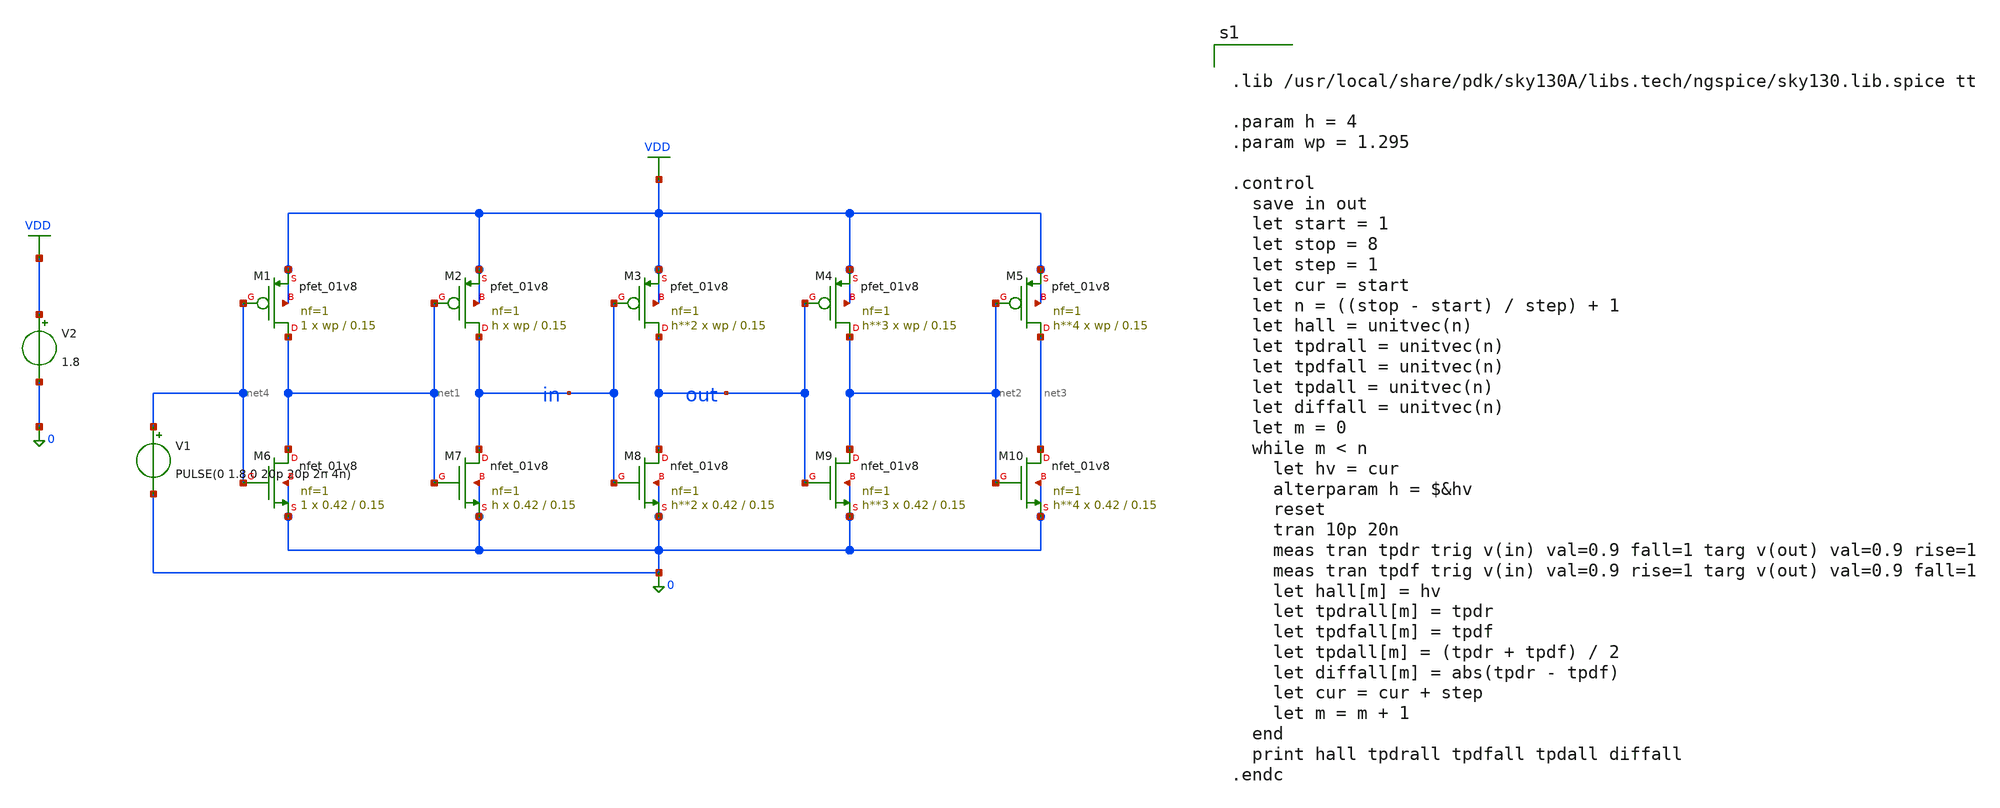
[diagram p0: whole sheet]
** sch_path: static_cmos/logicaleffort/inv.sch
**.subckt inv
V1 net4 0 PULSE(0 1.8 0 20p 20p 2n 4n)
V2 VDD 0 1.8
XM1 net1 net4 VDD VDD sky130_fd_pr__pfet_01v8 L=0.15 W=wp nf=1 ad='int((1 + 1)/2) * wp / 1 * 0.29' as='int((1 + 2)/2) * wp / 1 * 0.29'
+ pd='2*int((1 + 1)/2) * (wp / 1 + 0.29)' ps='2*int((1 + 2)/2) * (wp / 1 + 0.29)' nrd='0.29 / wp ' nrs='0.29 / wp '
+ sa=0 sb=0 sd=0 mult=1 m=1
XM2 in net1 VDD VDD sky130_fd_pr__pfet_01v8 L=0.15 W=wp nf=1 ad='int((1 + 1)/2) * wp / 1 * 0.29' as='int((1 + 2)/2) * wp / 1 * 0.29'
+ pd='2*int((1 + 1)/2) * (wp / 1 + 0.29)' ps='2*int((1 + 2)/2) * (wp / 1 + 0.29)' nrd='0.29 / wp ' nrs='0.29 / wp '
+ sa=0 sb=0 sd=0 mult=h m=h
XM3 out in VDD VDD sky130_fd_pr__pfet_01v8 L=0.15 W=wp nf=1 ad='int((1 + 1)/2) * wp / 1 * 0.29' as='int((1 + 2)/2) * wp / 1 * 0.29'
+ pd='2*int((1 + 1)/2) * (wp / 1 + 0.29)' ps='2*int((1 + 2)/2) * (wp / 1 + 0.29)' nrd='0.29 / wp ' nrs='0.29 / wp '
+ sa=0 sb=0 sd=0 mult=h**2 m=h**2
XM4 net2 out VDD VDD sky130_fd_pr__pfet_01v8 L=0.15 W=wp nf=1 ad='int((1 + 1)/2) * wp / 1 * 0.29' as='int((1 + 2)/2) * wp / 1 * 0.29'
+ pd='2*int((1 + 1)/2) * (wp / 1 + 0.29)' ps='2*int((1 + 2)/2) * (wp / 1 + 0.29)' nrd='0.29 / wp ' nrs='0.29 / wp '
+ sa=0 sb=0 sd=0 mult=h**3 m=h**3
XM5 net3 net2 VDD VDD sky130_fd_pr__pfet_01v8 L=0.15 W=wp nf=1 ad='int((1 + 1)/2) * wp / 1 * 0.29' as='int((1 + 2)/2) * wp / 1 * 0.29'
+ pd='2*int((1 + 1)/2) * (wp / 1 + 0.29)' ps='2*int((1 + 2)/2) * (wp / 1 + 0.29)' nrd='0.29 / wp ' nrs='0.29 / wp '
+ sa=0 sb=0 sd=0 mult=h**4 m=h**4
XM6 net1 net4 0 0 sky130_fd_pr__nfet_01v8 L=0.15 W=0.42 nf=1 ad='int((1 + 1)/2) * 0.42 / 1 * 0.29' as='int((1 + 2)/2) * 0.42 / 1 * 0.29'
+ pd='2*int((1 + 1)/2) * (0.42 / 1 + 0.29)' ps='2*int((1 + 2)/2) * (0.42 / 1 + 0.29)' nrd='0.29 / 0.42 '
+ nrs='0.29 / 0.42 ' sa=0 sb=0 sd=0 mult=1 m=1
XM7 in net1 0 0 sky130_fd_pr__nfet_01v8 L=0.15 W=0.42 nf=1 ad='int((1 + 1)/2) * 0.42 / 1 * 0.29' as='int((1 + 2)/2) * 0.42 / 1 * 0.29'
+ pd='2*int((1 + 1)/2) * (0.42 / 1 + 0.29)' ps='2*int((1 + 2)/2) * (0.42 / 1 + 0.29)' nrd='0.29 / 0.42 '
+ nrs='0.29 / 0.42 ' sa=0 sb=0 sd=0 mult=h m=h
XM8 out in 0 0 sky130_fd_pr__nfet_01v8 L=0.15 W=0.42 nf=1 ad='int((1 + 1)/2) * 0.42 / 1 * 0.29' as='int((1 + 2)/2) * 0.42 / 1 * 0.29'
+ pd='2*int((1 + 1)/2) * (0.42 / 1 + 0.29)' ps='2*int((1 + 2)/2) * (0.42 / 1 + 0.29)' nrd='0.29 / 0.42 '
+ nrs='0.29 / 0.42 ' sa=0 sb=0 sd=0 mult=h**2 m=h**2
XM9 net2 out 0 0 sky130_fd_pr__nfet_01v8 L=0.15 W=0.42 nf=1 ad='int((1 + 1)/2) * 0.42 / 1 * 0.29' as='int((1 + 2)/2) * 0.42 / 1 * 0.29'
+ pd='2*int((1 + 1)/2) * (0.42 / 1 + 0.29)' ps='2*int((1 + 2)/2) * (0.42 / 1 + 0.29)' nrd='0.29 / 0.42 '
+ nrs='0.29 / 0.42 ' sa=0 sb=0 sd=0 mult=h**3 m=h**3
XM10 net3 net2 0 0 sky130_fd_pr__nfet_01v8 L=0.15 W=0.42 nf=1 ad='int((1 + 1)/2) * 0.42 / 1 * 0.29' as='int((1 + 2)/2) * 0.42 / 1 * 0.29'
+ pd='2*int((1 + 1)/2) * (0.42 / 1 + 0.29)' ps='2*int((1 + 2)/2) * (0.42 / 1 + 0.29)' nrd='0.29 / 0.42 '
+ nrs='0.29 / 0.42 ' sa=0 sb=0 sd=0 mult=h**4 m=h**4
**** begin user architecture code


.lib /usr/local/share/pdk/sky130A/libs.tech/ngspice/sky130.lib.spice tt

.param h = 4
.param wp = 1.295

.control
  save in out
  let start = 1
  let stop = 8
  let step = 1
  let cur = start
  let n = ((stop - start) / step) + 1
  let hall = unitvec(n)
  let tpdrall = unitvec(n)
  let tpdfall = unitvec(n)
  let tpdall = unitvec(n)
  let diffall = unitvec(n)
  let m = 0
  while m < n
    let hv = cur
    alterparam h = $&hv
    reset
    tran 10p 20n
    meas tran tpdr trig v(in) val=0.9 fall=1 targ v(out) val=0.9 rise=1
    meas tran tpdf trig v(in) val=0.9 rise=1 targ v(out) val=0.9 fall=1
    let hall[m] = hv
    let tpdrall[m] = tpdr
    let tpdfall[m] = tpdf
    let tpdall[m] = (tpdr + tpdf) / 2
    let diffall[m] = abs(tpdr - tpdf)
    let cur = cur + step
    let m = m + 1
  end
  print hall tpdrall tpdfall tpdall diffall
.endc


**** end user architecture code
**.ends
.GLOBAL VDD
.end
